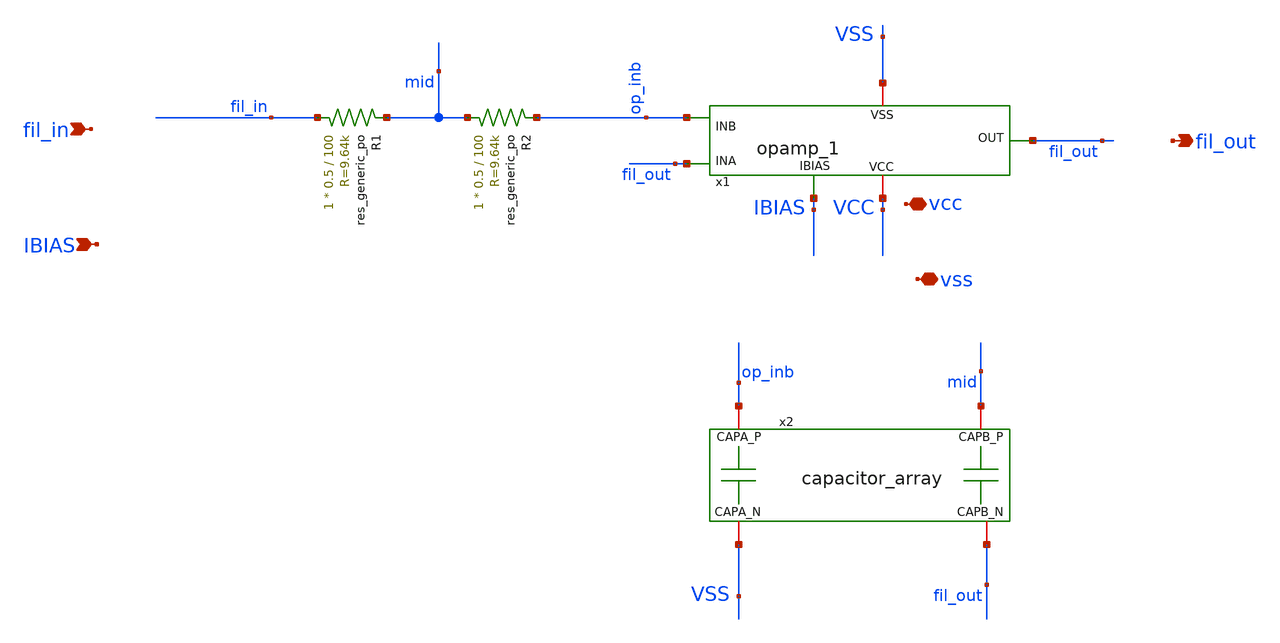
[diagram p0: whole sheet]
** sch_path: xschem/filter22M.sch
**.subckt filter22M fil_out fil_in vcc vss IBIAS
*.opin fil_out
*.ipin fil_in
*.iopin vcc
*.iopin vss
*.ipin IBIAS
x1 VCC fil_out fil_out op_inb VSS IBIAS opamp_1
XR1 fil_in mid sky130_fd_pr__res_generic_po W=0.5 L=100 m=1
XR2 mid op_inb sky130_fd_pr__res_generic_po W=0.5 L=100 m=1
x2 op_inb mid VSS fil_out capacitor_array
**.ends

* expanding   symbol:  opamp_1.sym # of pins=6
** sym_path: xschem/opamp_1.sym
** sch_path: xschem/opamp_1.sch
.subckt opamp_1 VCC OUT INA INB VSS IBIAS
*.ipin INA
*.ipin INB
*.opin OUT
*.iopin VCC
*.iopin VSS
*.ipin IBIAS
XM1 MIRR INA TAILV VSS sky130_fd_pr__nfet_01v8 L=1 W=20 nf=1 ad='int((nf+1)/2) * W/nf * 0.29' as='int((nf+2)/2) * W/nf * 0.29'
+ pd='2*int((nf+1)/2) * (W/nf + 0.29)' ps='2*int((nf+2)/2) * (W/nf + 0.29)' nrd='0.29 / W' nrs='0.29 / W'
+ sa=0 sb=0 sd=0 mult=1 m=1
XM2 DIFF_OUT INB TAILV VSS sky130_fd_pr__nfet_01v8 L=1 W=20 nf=1 ad='int((nf+1)/2) * W/nf * 0.29' as='int((nf+2)/2) * W/nf * 0.29'
+ pd='2*int((nf+1)/2) * (W/nf + 0.29)' ps='2*int((nf+2)/2) * (W/nf + 0.29)' nrd='0.29 / W' nrs='0.29 / W'
+ sa=0 sb=0 sd=0 mult=1 m=1
XM3 TAILV IBIAS VSS VSS sky130_fd_pr__nfet_01v8 L=1 W=40 nf=1 ad='int((nf+1)/2) * W/nf * 0.29' as='int((nf+2)/2) * W/nf * 0.29'
+ pd='2*int((nf+1)/2) * (W/nf + 0.29)' ps='2*int((nf+2)/2) * (W/nf + 0.29)' nrd='0.29 / W' nrs='0.29 / W'
+ sa=0 sb=0 sd=0 mult=1 m=1
XM4 MIRR MIRR VCC VCC sky130_fd_pr__pfet_01v8_lvt L=0.5 W=14 nf=1 ad='int((nf+1)/2) * W/nf * 0.29' as='int((nf+2)/2) * W/nf * 0.29'
+ pd='2*int((nf+1)/2) * (W/nf + 0.29)' ps='2*int((nf+2)/2) * (W/nf + 0.29)' nrd='0.29 / W' nrs='0.29 / W'
+ sa=0 sb=0 sd=0 mult=1 m=1
XM5 DIFF_OUT MIRR VCC VCC sky130_fd_pr__pfet_01v8_lvt L=0.5 W=14 nf=1 ad='int((nf+1)/2) * W/nf * 0.29'
+ as='int((nf+2)/2) * W/nf * 0.29' pd='2*int((nf+1)/2) * (W/nf + 0.29)' ps='2*int((nf+2)/2) * (W/nf + 0.29)'
+ nrd='0.29 / W' nrs='0.29 / W' sa=0 sb=0 sd=0 mult=1 m=1
XM6 OUT IBIAS VSS VSS sky130_fd_pr__nfet_01v8 L=0.5 W=93 nf=1 ad='int((nf+1)/2) * W/nf * 0.29' as='int((nf+2)/2) * W/nf * 0.29'
+ pd='2*int((nf+1)/2) * (W/nf + 0.29)' ps='2*int((nf+2)/2) * (W/nf + 0.29)' nrd='0.29 / W' nrs='0.29 / W'
+ sa=0 sb=0 sd=0 mult=1 m=1
XM7 OUT DIFF_OUT VCC VCC sky130_fd_pr__pfet_01v8_lvt L=0.5 W=70 nf=1 ad='int((nf+1)/2) * W/nf * 0.29'
+ as='int((nf+2)/2) * W/nf * 0.29' pd='2*int((nf+1)/2) * (W/nf + 0.29)' ps='2*int((nf+2)/2) * (W/nf + 0.29)'
+ nrd='0.29 / W' nrs='0.29 / W' sa=0 sb=0 sd=0 mult=1 m=1
XM9 RBIAS IBIAS VSS VSS sky130_fd_pr__nfet_01v8 L=1 W=5 nf=1 ad='int((nf+1)/2) * W/nf * 0.29' as='int((nf+2)/2) * W/nf * 0.29'
+ pd='2*int((nf+1)/2) * (W/nf + 0.29)' ps='2*int((nf+2)/2) * (W/nf + 0.29)' nrd='0.29 / W' nrs='0.29 / W'
+ sa=0 sb=0 sd=0 mult=1 m=1
XM10 RBIAS RBIAS net2 VCC sky130_fd_pr__pfet_01v8_lvt L=0.5 W=1 nf=1 ad='int((nf+1)/2) * W/nf * 0.29'
+ as='int((nf+2)/2) * W/nf * 0.29' pd='2*int((nf+1)/2) * (W/nf + 0.29)' ps='2*int((nf+2)/2) * (W/nf + 0.29)'
+ nrd='0.29 / W' nrs='0.29 / W' sa=0 sb=0 sd=0 mult=1 m=1
XM11 net2 net2 VCC VCC sky130_fd_pr__pfet_01v8_lvt L=0.5 W=7.5 nf=1 ad='int((nf+1)/2) * W/nf * 0.29'
+ as='int((nf+2)/2) * W/nf * 0.29' pd='2*int((nf+1)/2) * (W/nf + 0.29)' ps='2*int((nf+2)/2) * (W/nf + 0.29)'
+ nrd='0.29 / W' nrs='0.29 / W' sa=0 sb=0 sd=0 mult=1 m=1
XC1 OUT net1 sky130_fd_pr__cap_mim_m3_2 W=20 L=13 MF=1 m=1
XM8 net1 RBIAS DIFF_OUT VCC sky130_fd_pr__pfet_01v8_lvt L=0.5 W=14 nf=1 ad='int((nf+1)/2) * W/nf * 0.29'
+ as='int((nf+2)/2) * W/nf * 0.29' pd='2*int((nf+1)/2) * (W/nf + 0.29)' ps='2*int((nf+2)/2) * (W/nf + 0.29)'
+ nrd='0.29 / W' nrs='0.29 / W' sa=0 sb=0 sd=0 mult=1 m=1
.ends


* expanding   symbol:  capacitor_array.sym # of pins=4
** sym_path: xschem/capacitor_array.sym
** sch_path: xschem/capacitor_array.sch
.subckt capacitor_array CAPA_P CAPB_P CAPA_N CAPB_N
*.iopin CAPA_P
*.iopin CAPA_N
*.iopin CAPB_P
*.iopin CAPB_N
XC13 CAPA_P CAPA_N sky130_fd_pr__cap_mim_m3_1 W=10 L=6 MF=1 m=1
XC1 CAPA_P CAPA_N sky130_fd_pr__cap_mim_m3_1 W=10 L=6 MF=1 m=1
XC2 CAPA_P CAPA_N sky130_fd_pr__cap_mim_m3_1 W=10 L=6 MF=1 m=1
XC3 CAPA_P CAPA_N sky130_fd_pr__cap_mim_m3_1 W=10 L=6 MF=1 m=1
XC4 CAPB_P CAPB_N sky130_fd_pr__cap_mim_m3_1 W=10 L=6 MF=1 m=1
XC5 CAPB_P CAPB_N sky130_fd_pr__cap_mim_m3_1 W=10 L=6 MF=1 m=1
XC6 CAPB_P CAPB_N sky130_fd_pr__cap_mim_m3_1 W=10 L=6 MF=1 m=1
XC7 CAPB_P CAPB_N sky130_fd_pr__cap_mim_m3_1 W=10 L=6 MF=1 m=1
XC8 CAPB_P CAPB_N sky130_fd_pr__cap_mim_m3_1 W=10 L=6 MF=1 m=1
XC9 CAPB_P CAPB_N sky130_fd_pr__cap_mim_m3_1 W=10 L=6 MF=1 m=1
XC10 CAPB_P CAPB_N sky130_fd_pr__cap_mim_m3_1 W=10 L=6 MF=1 m=1
XC11 CAPB_P CAPB_N sky130_fd_pr__cap_mim_m3_1 W=10 L=6 MF=1 m=1
.ends

.end
